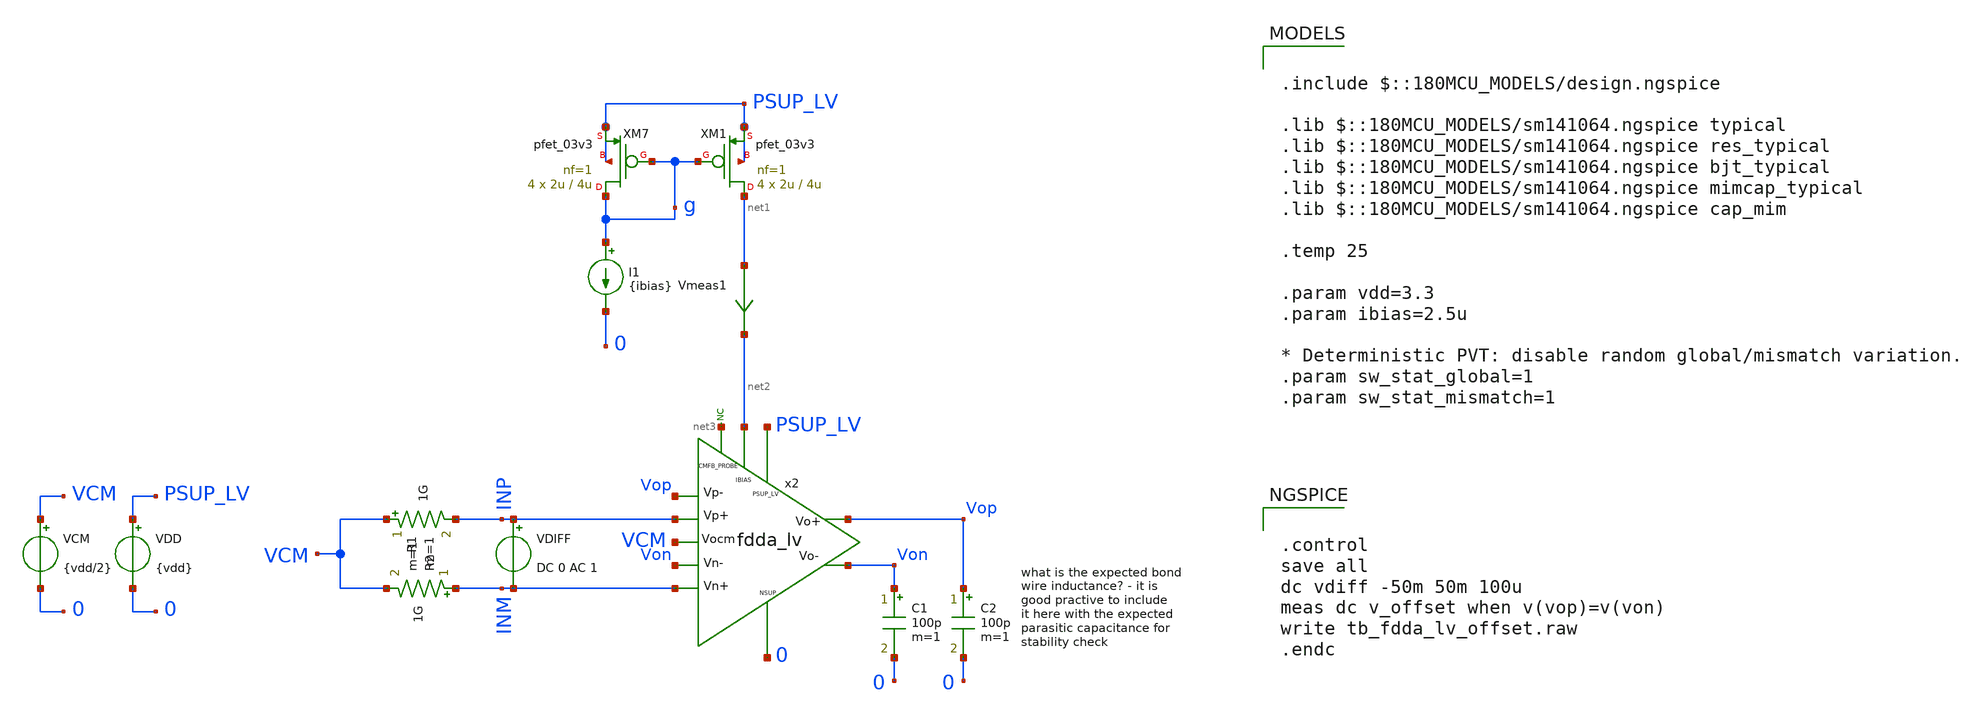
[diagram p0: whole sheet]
** sch_path: xschem/blocks/fdda_lv/tb_fdda_lv_offset.sch
**.subckt tb_fdda_lv_offset
C1 Von 0 100p m=1
x2 PSUP_LV Vop Von INM INP Vop Von net2 0 net3 VCM fdda_lv
VDD PSUP_LV 0 {vdd}
C2 Vop 0 100p m=1
VCM VCM 0 {vdd/2}
* noconn #net3
VDIFF INP INM DC 0 AC 1
R1 VCM INP 1G m=1
R2 INM VCM 1G m=1
XM7 g g PSUP_LV PSUP_LV pfet_03v3 L=4u W=2u nf=1 ad='int((nf+1)/2) * W/nf * 0.18u' as='int((nf+2)/2) * W/nf * 0.18u'
+ pd='2*int((nf+1)/2) * (W/nf + 0.18u)' ps='2*int((nf+2)/2) * (W/nf + 0.18u)' nrd='0.18u / W' nrs='0.18u / W'
+ sa=0 sb=0 sd=0 m=4
XM1 net1 g PSUP_LV PSUP_LV pfet_03v3 L=4u W=2u nf=1 ad='int((nf+1)/2) * W/nf * 0.18u' as='int((nf+2)/2) * W/nf * 0.18u'
+ pd='2*int((nf+1)/2) * (W/nf + 0.18u)' ps='2*int((nf+2)/2) * (W/nf + 0.18u)' nrd='0.18u / W' nrs='0.18u / W'
+ sa=0 sb=0 sd=0 m=4
I1 g 0 {ibias}
Vmeas1 net1 net2 0
.save i(vmeas1)
**** begin user architecture code

.include $::180MCU_MODELS/design.ngspice

.lib $::180MCU_MODELS/sm141064.ngspice typical
.lib $::180MCU_MODELS/sm141064.ngspice res_typical
.lib $::180MCU_MODELS/sm141064.ngspice bjt_typical
.lib $::180MCU_MODELS/sm141064.ngspice mimcap_typical
.lib $::180MCU_MODELS/sm141064.ngspice cap_mim

.temp 25

.param vdd=3.3
.param ibias=2.5u

* Deterministic PVT: disable random global/mismatch variation.
.param sw_stat_global=1
.param sw_stat_mismatch=1



.control
save all
dc vdiff -50m 50m 100u
meas dc v_offset when v(vop)=v(von)
write tb_fdda_lv_offset.raw
.endc


**** end user architecture code
**.ends
.end
